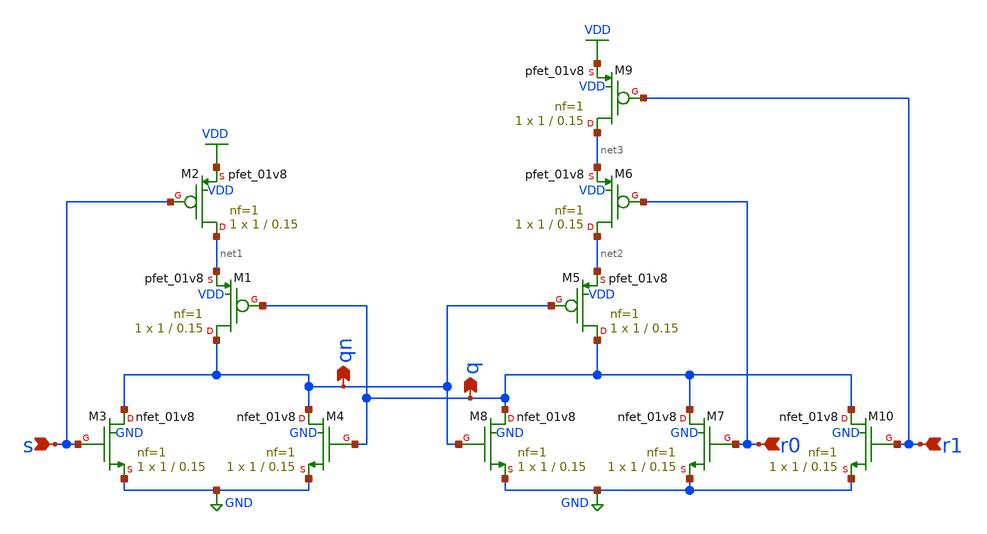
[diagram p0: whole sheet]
** sch_path: xschem/sr_latch.sch
**.subckt sr_latch s r0 qn q r1
*.ipin s
*.ipin r0
*.opin qn
*.opin q
*.ipin r1
XM1 qn q net1 VDD sky130_fd_pr__pfet_01v8 L=0.15 W=1 nf=1 ad='int((1 + 1)/2) * 1 / 1 * 0.29' as='int((1 + 2)/2) * 1 / 1 * 0.29'
+ pd='2*int((1 + 1)/2) * (1 / 1 + 0.29)' ps='2*int((1 + 2)/2) * (1 / 1 + 0.29)' nrd='0.29 / 1 ' nrs='0.29 / 1 '
+ sa=0 sb=0 sd=0 mult=1 m=1
XM2 net1 s VDD VDD sky130_fd_pr__pfet_01v8 L=0.15 W=1 nf=1 ad='int((1 + 1)/2) * 1 / 1 * 0.29' as='int((1 + 2)/2) * 1 / 1 * 0.29'
+ pd='2*int((1 + 1)/2) * (1 / 1 + 0.29)' ps='2*int((1 + 2)/2) * (1 / 1 + 0.29)' nrd='0.29 / 1 ' nrs='0.29 / 1 '
+ sa=0 sb=0 sd=0 mult=1 m=1
XM3 qn s GND GND sky130_fd_pr__nfet_01v8 L=0.15 W=1 nf=1 ad='int((1 + 1)/2) * 1 / 1 * 0.29' as='int((1 + 2)/2) * 1 / 1 * 0.29'
+ pd='2*int((1 + 1)/2) * (1 / 1 + 0.29)' ps='2*int((1 + 2)/2) * (1 / 1 + 0.29)' nrd='0.29 / 1 ' nrs='0.29 / 1 '
+ sa=0 sb=0 sd=0 mult=1 m=1
XM4 qn q GND GND sky130_fd_pr__nfet_01v8 L=0.15 W=1 nf=1 ad='int((1 + 1)/2) * 1 / 1 * 0.29' as='int((1 + 2)/2) * 1 / 1 * 0.29'
+ pd='2*int((1 + 1)/2) * (1 / 1 + 0.29)' ps='2*int((1 + 2)/2) * (1 / 1 + 0.29)' nrd='0.29 / 1 ' nrs='0.29 / 1 '
+ sa=0 sb=0 sd=0 mult=1 m=1
XM5 q qn net2 VDD sky130_fd_pr__pfet_01v8 L=0.15 W=1 nf=1 ad='int((1 + 1)/2) * 1 / 1 * 0.29' as='int((1 + 2)/2) * 1 / 1 * 0.29'
+ pd='2*int((1 + 1)/2) * (1 / 1 + 0.29)' ps='2*int((1 + 2)/2) * (1 / 1 + 0.29)' nrd='0.29 / 1 ' nrs='0.29 / 1 '
+ sa=0 sb=0 sd=0 mult=1 m=1
XM6 net2 r0 net3 VDD sky130_fd_pr__pfet_01v8 L=0.15 W=1 nf=1 ad='int((1 + 1)/2) * 1 / 1 * 0.29' as='int((1 + 2)/2) * 1 / 1 * 0.29'
+ pd='2*int((1 + 1)/2) * (1 / 1 + 0.29)' ps='2*int((1 + 2)/2) * (1 / 1 + 0.29)' nrd='0.29 / 1 ' nrs='0.29 / 1 '
+ sa=0 sb=0 sd=0 mult=1 m=1
XM7 q r0 GND GND sky130_fd_pr__nfet_01v8 L=0.15 W=1 nf=1 ad='int((1 + 1)/2) * 1 / 1 * 0.29' as='int((1 + 2)/2) * 1 / 1 * 0.29'
+ pd='2*int((1 + 1)/2) * (1 / 1 + 0.29)' ps='2*int((1 + 2)/2) * (1 / 1 + 0.29)' nrd='0.29 / 1 ' nrs='0.29 / 1 '
+ sa=0 sb=0 sd=0 mult=1 m=1
XM8 q qn GND GND sky130_fd_pr__nfet_01v8 L=0.15 W=1 nf=1 ad='int((1 + 1)/2) * 1 / 1 * 0.29' as='int((1 + 2)/2) * 1 / 1 * 0.29'
+ pd='2*int((1 + 1)/2) * (1 / 1 + 0.29)' ps='2*int((1 + 2)/2) * (1 / 1 + 0.29)' nrd='0.29 / 1 ' nrs='0.29 / 1 '
+ sa=0 sb=0 sd=0 mult=1 m=1
XM9 net3 r1 VDD VDD sky130_fd_pr__pfet_01v8 L=0.15 W=1 nf=1 ad='int((1 + 1)/2) * 1 / 1 * 0.29' as='int((1 + 2)/2) * 1 / 1 * 0.29'
+ pd='2*int((1 + 1)/2) * (1 / 1 + 0.29)' ps='2*int((1 + 2)/2) * (1 / 1 + 0.29)' nrd='0.29 / 1 ' nrs='0.29 / 1 '
+ sa=0 sb=0 sd=0 mult=1 m=1
XM10 q r1 GND GND sky130_fd_pr__nfet_01v8 L=0.15 W=1 nf=1 ad='int((1 + 1)/2) * 1 / 1 * 0.29' as='int((1 + 2)/2) * 1 / 1 * 0.29'
+ pd='2*int((1 + 1)/2) * (1 / 1 + 0.29)' ps='2*int((1 + 2)/2) * (1 / 1 + 0.29)' nrd='0.29 / 1 ' nrs='0.29 / 1 '
+ sa=0 sb=0 sd=0 mult=1 m=1
**.ends
.GLOBAL VDD
.GLOBAL GND
.end
